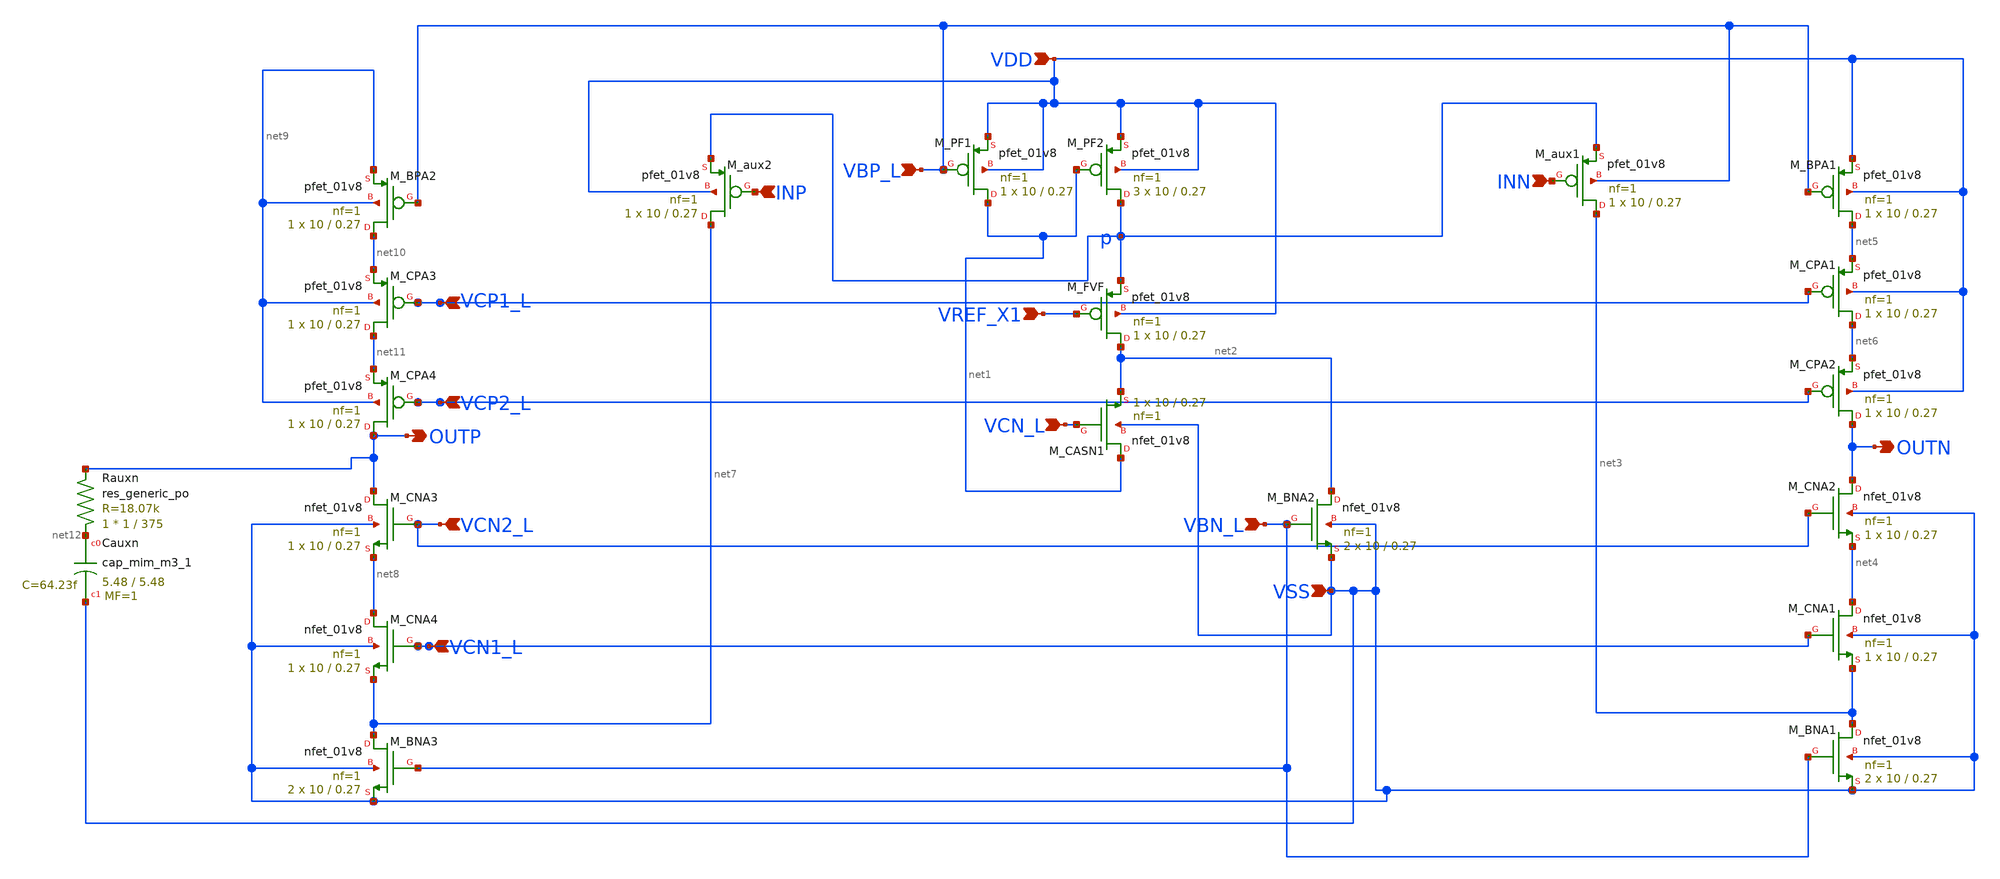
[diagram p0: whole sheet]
** sch_path: auxp.sch
**.subckt auxp VSS VDD VBN_L VCN_L VBP_L VREF_X1 INN INP VCP1_L VCP2_L VCN1_L VCN2_L OUTP OUTN
*.ipin VSS
*.ipin VDD
*.ipin VBN_L
*.ipin VCN_L
*.ipin VBP_L
*.ipin VREF_X1
*.ipin INN
*.ipin INP
*.ipin VCP1_L
*.ipin VCP2_L
*.ipin VCN1_L
*.ipin VCN2_L
*.opin OUTP
*.opin OUTN
XM_BNA2 net2 VBN_L VSS VSS sky130_fd_pr__nfet_01v8 L=0.27 W=10 nf=1 ad='int((1 + 1)/2) * 10 / 1 * 0.29'
+ as='int((1 + 2)/2) * 10 / 1 * 0.29' pd='2*int((1 + 1)/2) * (10 / 1 + 0.29)' ps='2*int((1 + 2)/2) * (10 / 1 + 0.29)'
+ nrd='0.29 / 10 ' nrs='0.29 / 10 ' sa=0 sb=0 sd=0 mult=2 m=2
XM_FVF net2 VREF_X1 p VDD sky130_fd_pr__pfet_01v8 L=0.27 W=10 nf=1 ad='int((1 + 1)/2) * 10 / 1 * 0.29'
+ as='int((1 + 2)/2) * 10 / 1 * 0.29' pd='2*int((1 + 1)/2) * (10 / 1 + 0.29)' ps='2*int((1 + 2)/2) * (10 / 1 + 0.29)'
+ nrd='0.29 / 10 ' nrs='0.29 / 10 ' sa=0 sb=0 sd=0 mult=1 m=1
XM_PF1 net1 VBP_L VDD VDD sky130_fd_pr__pfet_01v8 L=0.27 W=10 nf=1 ad='int((1 + 1)/2) * 10 / 1 * 0.29'
+ as='int((1 + 2)/2) * 10 / 1 * 0.29' pd='2*int((1 + 1)/2) * (10 / 1 + 0.29)' ps='2*int((1 + 2)/2) * (10 / 1 + 0.29)'
+ nrd='0.29 / 10 ' nrs='0.29 / 10 ' sa=0 sb=0 sd=0 mult=1 m=1
XM_PF2 p net1 VDD VDD sky130_fd_pr__pfet_01v8 L=0.27 W=10 nf=1 ad='int((1 + 1)/2) * 10 / 1 * 0.29' as='int((1 + 2)/2) * 10 / 1 * 0.29'
+ pd='2*int((1 + 1)/2) * (10 / 1 + 0.29)' ps='2*int((1 + 2)/2) * (10 / 1 + 0.29)' nrd='0.29 / 10 ' nrs='0.29 / 10 '
+ sa=0 sb=0 sd=0 mult=3 m=3
XM_CASN1 net1 VCN_L net2 VSS sky130_fd_pr__nfet_01v8 L=0.27 W=10 nf=1 ad='int((1 + 1)/2) * 10 / 1 * 0.29'
+ as='int((1 + 2)/2) * 10 / 1 * 0.29' pd='2*int((1 + 1)/2) * (10 / 1 + 0.29)' ps='2*int((1 + 2)/2) * (10 / 1 + 0.29)'
+ nrd='0.29 / 10 ' nrs='0.29 / 10 ' sa=0 sb=0 sd=0 mult=1 m=1
XM_aux1 net3 INN p VBP_L sky130_fd_pr__pfet_01v8 L=0.27 W=10 nf=1 ad='int((1 + 1)/2) * 10 / 1 * 0.29'
+ as='int((1 + 2)/2) * 10 / 1 * 0.29' pd='2*int((1 + 1)/2) * (10 / 1 + 0.29)' ps='2*int((1 + 2)/2) * (10 / 1 + 0.29)'
+ nrd='0.29 / 10 ' nrs='0.29 / 10 ' sa=0 sb=0 sd=0 mult=1 m=1
XM_BPA1 net5 VBP_L VDD VDD sky130_fd_pr__pfet_01v8 L=0.27 W=10 nf=1 ad='int((1 + 1)/2) * 10 / 1 * 0.29'
+ as='int((1 + 2)/2) * 10 / 1 * 0.29' pd='2*int((1 + 1)/2) * (10 / 1 + 0.29)' ps='2*int((1 + 2)/2) * (10 / 1 + 0.29)'
+ nrd='0.29 / 10 ' nrs='0.29 / 10 ' sa=0 sb=0 sd=0 mult=1 m=1
XM_CPA1 net6 VCP1_L net5 VDD sky130_fd_pr__pfet_01v8 L=0.27 W=10 nf=1 ad='int((1 + 1)/2) * 10 / 1 * 0.29'
+ as='int((1 + 2)/2) * 10 / 1 * 0.29' pd='2*int((1 + 1)/2) * (10 / 1 + 0.29)' ps='2*int((1 + 2)/2) * (10 / 1 + 0.29)'
+ nrd='0.29 / 10 ' nrs='0.29 / 10 ' sa=0 sb=0 sd=0 mult=1 m=1
XM_CPA2 OUTN VCP2_L net6 VDD sky130_fd_pr__pfet_01v8 L=0.27 W=10 nf=1 ad='int((1 + 1)/2) * 10 / 1 * 0.29'
+ as='int((1 + 2)/2) * 10 / 1 * 0.29' pd='2*int((1 + 1)/2) * (10 / 1 + 0.29)' ps='2*int((1 + 2)/2) * (10 / 1 + 0.29)'
+ nrd='0.29 / 10 ' nrs='0.29 / 10 ' sa=0 sb=0 sd=0 mult=1 m=1
XM_CNA2 OUTN VCN2_L net4 VSS sky130_fd_pr__nfet_01v8 L=0.27 W=10 nf=1 ad='int((1 + 1)/2) * 10 / 1 * 0.29'
+ as='int((1 + 2)/2) * 10 / 1 * 0.29' pd='2*int((1 + 1)/2) * (10 / 1 + 0.29)' ps='2*int((1 + 2)/2) * (10 / 1 + 0.29)'
+ nrd='0.29 / 10 ' nrs='0.29 / 10 ' sa=0 sb=0 sd=0 mult=1 m=1
XM_CNA1 net4 VCN1_L net3 VSS sky130_fd_pr__nfet_01v8 L=0.27 W=10 nf=1 ad='int((1 + 1)/2) * 10 / 1 * 0.29'
+ as='int((1 + 2)/2) * 10 / 1 * 0.29' pd='2*int((1 + 1)/2) * (10 / 1 + 0.29)' ps='2*int((1 + 2)/2) * (10 / 1 + 0.29)'
+ nrd='0.29 / 10 ' nrs='0.29 / 10 ' sa=0 sb=0 sd=0 mult=1 m=1
XM_BNA1 net3 VBN_L VSS VSS sky130_fd_pr__nfet_01v8 L=0.27 W=10 nf=1 ad='int((1 + 1)/2) * 10 / 1 * 0.29'
+ as='int((1 + 2)/2) * 10 / 1 * 0.29' pd='2*int((1 + 1)/2) * (10 / 1 + 0.29)' ps='2*int((1 + 2)/2) * (10 / 1 + 0.29)'
+ nrd='0.29 / 10 ' nrs='0.29 / 10 ' sa=0 sb=0 sd=0 mult=2 m=2
XM_aux2 net7 INP p VDD sky130_fd_pr__pfet_01v8 L=0.27 W=10 nf=1 ad='int((1 + 1)/2) * 10 / 1 * 0.29' as='int((1 + 2)/2) * 10 / 1 * 0.29'
+ pd='2*int((1 + 1)/2) * (10 / 1 + 0.29)' ps='2*int((1 + 2)/2) * (10 / 1 + 0.29)' nrd='0.29 / 10 ' nrs='0.29 / 10 '
+ sa=0 sb=0 sd=0 mult=1 m=1
XM_BPA2 net10 VBP_L net9 net9 sky130_fd_pr__pfet_01v8 L=0.27 W=10 nf=1 ad='int((1 + 1)/2) * 10 / 1 * 0.29'
+ as='int((1 + 2)/2) * 10 / 1 * 0.29' pd='2*int((1 + 1)/2) * (10 / 1 + 0.29)' ps='2*int((1 + 2)/2) * (10 / 1 + 0.29)'
+ nrd='0.29 / 10 ' nrs='0.29 / 10 ' sa=0 sb=0 sd=0 mult=1 m=1
XM_CPA3 net11 VCP1_L net10 net9 sky130_fd_pr__pfet_01v8 L=0.27 W=10 nf=1 ad='int((1 + 1)/2) * 10 / 1 * 0.29'
+ as='int((1 + 2)/2) * 10 / 1 * 0.29' pd='2*int((1 + 1)/2) * (10 / 1 + 0.29)' ps='2*int((1 + 2)/2) * (10 / 1 + 0.29)'
+ nrd='0.29 / 10 ' nrs='0.29 / 10 ' sa=0 sb=0 sd=0 mult=1 m=1
XM_CPA4 OUTP VCP2_L net11 net9 sky130_fd_pr__pfet_01v8 L=0.27 W=10 nf=1 ad='int((1 + 1)/2) * 10 / 1 * 0.29'
+ as='int((1 + 2)/2) * 10 / 1 * 0.29' pd='2*int((1 + 1)/2) * (10 / 1 + 0.29)' ps='2*int((1 + 2)/2) * (10 / 1 + 0.29)'
+ nrd='0.29 / 10 ' nrs='0.29 / 10 ' sa=0 sb=0 sd=0 mult=1 m=1
XM_CNA3 OUTP VCN2_L net8 VSS sky130_fd_pr__nfet_01v8 L=0.27 W=10 nf=1 ad='int((1 + 1)/2) * 10 / 1 * 0.29'
+ as='int((1 + 2)/2) * 10 / 1 * 0.29' pd='2*int((1 + 1)/2) * (10 / 1 + 0.29)' ps='2*int((1 + 2)/2) * (10 / 1 + 0.29)'
+ nrd='0.29 / 10 ' nrs='0.29 / 10 ' sa=0 sb=0 sd=0 mult=1 m=1
XM_CNA4 net8 VCN1_L net7 VSS sky130_fd_pr__nfet_01v8 L=0.27 W=10 nf=1 ad='int((1 + 1)/2) * 10 / 1 * 0.29'
+ as='int((1 + 2)/2) * 10 / 1 * 0.29' pd='2*int((1 + 1)/2) * (10 / 1 + 0.29)' ps='2*int((1 + 2)/2) * (10 / 1 + 0.29)'
+ nrd='0.29 / 10 ' nrs='0.29 / 10 ' sa=0 sb=0 sd=0 mult=1 m=1
XM_BNA3 net7 VBN_L VSS VSS sky130_fd_pr__nfet_01v8 L=0.27 W=10 nf=1 ad='int((1 + 1)/2) * 10 / 1 * 0.29'
+ as='int((1 + 2)/2) * 10 / 1 * 0.29' pd='2*int((1 + 1)/2) * (10 / 1 + 0.29)' ps='2*int((1 + 2)/2) * (10 / 1 + 0.29)'
+ nrd='0.29 / 10 ' nrs='0.29 / 10 ' sa=0 sb=0 sd=0 mult=2 m=2
XCauxn net12 VSS sky130_fd_pr__cap_mim_m3_1 W=5.48 L=5.48 MF=1 m=1
XRauxn net12 OUTP sky130_fd_pr__res_generic_po W=1 L=375 m=1
**.ends
.end
